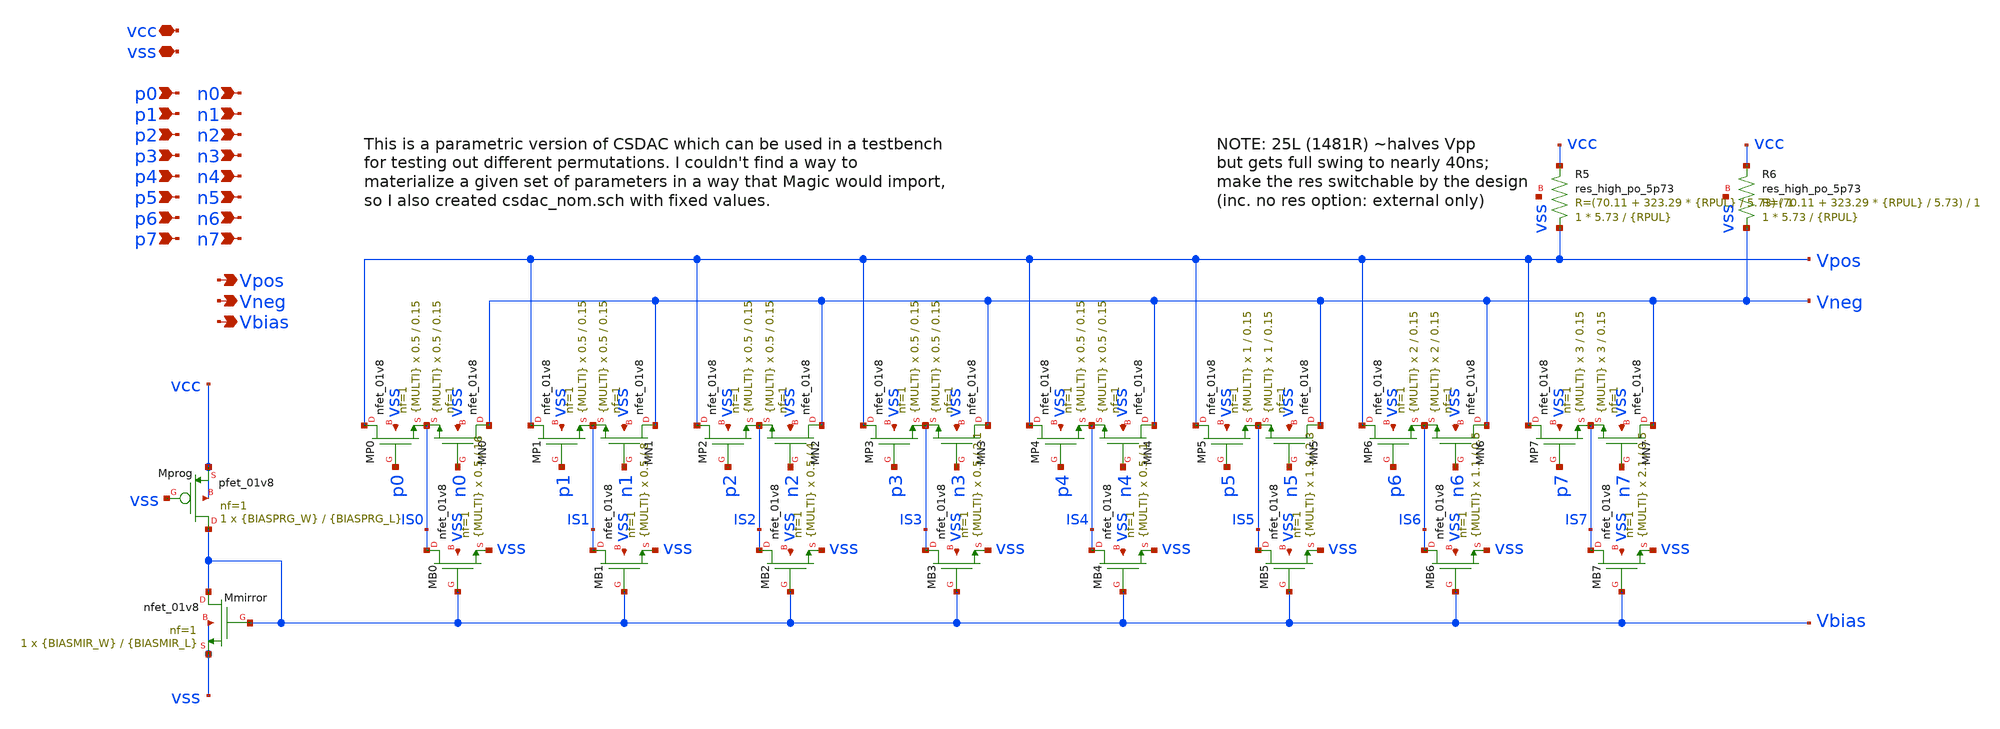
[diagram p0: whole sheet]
** sch_path: xschem/csdac.sch
**.subckt csdac vcc vss p0 n0 p1 n1 p2 n2 p3 n3 p4 n4 p5 n5 p6 n6 p7 n7 Vpos Vneg Vbias
*.iopin vcc
*.iopin vss
*.ipin p0
*.ipin n0
*.ipin p1
*.ipin n1
*.ipin p2
*.ipin n2
*.ipin p3
*.ipin n3
*.ipin p4
*.ipin n4
*.ipin p5
*.ipin n5
*.ipin p6
*.ipin n6
*.ipin p7
*.ipin n7
*.opin Vpos
*.opin Vneg
*.opin Vbias
XMprog Vbias vss vcc vcc sky130_fd_pr__pfet_01v8 L={BIASPRG_L} W={BIASPRG_W} nf=1 ad='int((nf+1)/2) * W/nf * 0.29'
+ as='int((nf+2)/2) * W/nf * 0.29' pd='2*int((nf+1)/2) * (W/nf + 0.29)' ps='2*int((nf+2)/2) * (W/nf + 0.29)'
+ nrd='0.29 / W' nrs='0.29 / W' sa=0 sb=0 sd=0 mult=1 m=1
XMmirror Vbias Vbias vss vss sky130_fd_pr__nfet_01v8 L={BIASMIR_L} W={BIASMIR_W} nf=1 ad='int((nf+1)/2) * W/nf * 0.29'
+ as='int((nf+2)/2) * W/nf * 0.29' pd='2*int((nf+1)/2) * (W/nf + 0.29)' ps='2*int((nf+2)/2) * (W/nf + 0.29)'
+ nrd='0.29 / W' nrs='0.29 / W' sa=0 sb=0 sd=0 mult=1 m=1
XMB0 IS0 Vbias vss vss sky130_fd_pr__nfet_01v8 L=16 W=0.5 nf=1 ad='int((nf+1)/2) * W/nf * 0.29' as='int((nf+2)/2) * W/nf * 0.29'
+ pd='2*int((nf+1)/2) * (W/nf + 0.29)' ps='2*int((nf+2)/2) * (W/nf + 0.29)' nrd='0.29 / W' nrs='0.29 / W'
+ sa=0 sb=0 sd=0 mult={MULTI} m={MULTI}
XMP0 Vpos p0 IS0 vss sky130_fd_pr__nfet_01v8 L=0.15 W=0.5 nf=1 ad='int((nf+1)/2) * W/nf * 0.29' as='int((nf+2)/2) * W/nf * 0.29'
+ pd='2*int((nf+1)/2) * (W/nf + 0.29)' ps='2*int((nf+2)/2) * (W/nf + 0.29)' nrd='0.29 / W' nrs='0.29 / W'
+ sa=0 sb=0 sd=0 mult={MULTI} m={MULTI}
XMN0 Vneg n0 IS0 vss sky130_fd_pr__nfet_01v8 L=0.15 W=0.5 nf=1 ad='int((nf+1)/2) * W/nf * 0.29' as='int((nf+2)/2) * W/nf * 0.29'
+ pd='2*int((nf+1)/2) * (W/nf + 0.29)' ps='2*int((nf+2)/2) * (W/nf + 0.29)' nrd='0.29 / W' nrs='0.29 / W'
+ sa=0 sb=0 sd=0 mult={MULTI} m={MULTI}
XMB1 IS1 Vbias vss vss sky130_fd_pr__nfet_01v8 L=8 W=0.5 nf=1 ad='int((nf+1)/2) * W/nf * 0.29' as='int((nf+2)/2) * W/nf * 0.29'
+ pd='2*int((nf+1)/2) * (W/nf + 0.29)' ps='2*int((nf+2)/2) * (W/nf + 0.29)' nrd='0.29 / W' nrs='0.29 / W'
+ sa=0 sb=0 sd=0 mult={MULTI} m={MULTI}
XMP1 Vpos p1 IS1 vss sky130_fd_pr__nfet_01v8 L=0.15 W=0.5 nf=1 ad='int((nf+1)/2) * W/nf * 0.29' as='int((nf+2)/2) * W/nf * 0.29'
+ pd='2*int((nf+1)/2) * (W/nf + 0.29)' ps='2*int((nf+2)/2) * (W/nf + 0.29)' nrd='0.29 / W' nrs='0.29 / W'
+ sa=0 sb=0 sd=0 mult={MULTI} m={MULTI}
XMN1 Vneg n1 IS1 vss sky130_fd_pr__nfet_01v8 L=0.15 W=0.5 nf=1 ad='int((nf+1)/2) * W/nf * 0.29' as='int((nf+2)/2) * W/nf * 0.29'
+ pd='2*int((nf+1)/2) * (W/nf + 0.29)' ps='2*int((nf+2)/2) * (W/nf + 0.29)' nrd='0.29 / W' nrs='0.29 / W'
+ sa=0 sb=0 sd=0 mult={MULTI} m={MULTI}
XMB2 IS2 Vbias vss vss sky130_fd_pr__nfet_01v8 L=4 W=0.5 nf=1 ad='int((nf+1)/2) * W/nf * 0.29' as='int((nf+2)/2) * W/nf * 0.29'
+ pd='2*int((nf+1)/2) * (W/nf + 0.29)' ps='2*int((nf+2)/2) * (W/nf + 0.29)' nrd='0.29 / W' nrs='0.29 / W'
+ sa=0 sb=0 sd=0 mult={MULTI} m={MULTI}
XMP2 Vpos p2 IS2 vss sky130_fd_pr__nfet_01v8 L=0.15 W=0.5 nf=1 ad='int((nf+1)/2) * W/nf * 0.29' as='int((nf+2)/2) * W/nf * 0.29'
+ pd='2*int((nf+1)/2) * (W/nf + 0.29)' ps='2*int((nf+2)/2) * (W/nf + 0.29)' nrd='0.29 / W' nrs='0.29 / W'
+ sa=0 sb=0 sd=0 mult={MULTI} m={MULTI}
XMN2 Vneg n2 IS2 vss sky130_fd_pr__nfet_01v8 L=0.15 W=0.5 nf=1 ad='int((nf+1)/2) * W/nf * 0.29' as='int((nf+2)/2) * W/nf * 0.29'
+ pd='2*int((nf+1)/2) * (W/nf + 0.29)' ps='2*int((nf+2)/2) * (W/nf + 0.29)' nrd='0.29 / W' nrs='0.29 / W'
+ sa=0 sb=0 sd=0 mult={MULTI} m={MULTI}
XMB3 IS3 Vbias vss vss sky130_fd_pr__nfet_01v8 L=2.1 W=0.5 nf=1 ad='int((nf+1)/2) * W/nf * 0.29' as='int((nf+2)/2) * W/nf * 0.29'
+ pd='2*int((nf+1)/2) * (W/nf + 0.29)' ps='2*int((nf+2)/2) * (W/nf + 0.29)' nrd='0.29 / W' nrs='0.29 / W'
+ sa=0 sb=0 sd=0 mult={MULTI} m={MULTI}
XMP3 Vpos p3 IS3 vss sky130_fd_pr__nfet_01v8 L=0.15 W=0.5 nf=1 ad='int((nf+1)/2) * W/nf * 0.29' as='int((nf+2)/2) * W/nf * 0.29'
+ pd='2*int((nf+1)/2) * (W/nf + 0.29)' ps='2*int((nf+2)/2) * (W/nf + 0.29)' nrd='0.29 / W' nrs='0.29 / W'
+ sa=0 sb=0 sd=0 mult={MULTI} m={MULTI}
XMN3 Vneg n3 IS3 vss sky130_fd_pr__nfet_01v8 L=0.15 W=0.5 nf=1 ad='int((nf+1)/2) * W/nf * 0.29' as='int((nf+2)/2) * W/nf * 0.29'
+ pd='2*int((nf+1)/2) * (W/nf + 0.29)' ps='2*int((nf+2)/2) * (W/nf + 0.29)' nrd='0.29 / W' nrs='0.29 / W'
+ sa=0 sb=0 sd=0 mult={MULTI} m={MULTI}
XMB4 IS4 Vbias vss vss sky130_fd_pr__nfet_01v8 L=1 W=0.5 nf=1 ad='int((nf+1)/2) * W/nf * 0.29' as='int((nf+2)/2) * W/nf * 0.29'
+ pd='2*int((nf+1)/2) * (W/nf + 0.29)' ps='2*int((nf+2)/2) * (W/nf + 0.29)' nrd='0.29 / W' nrs='0.29 / W'
+ sa=0 sb=0 sd=0 mult={MULTI} m={MULTI}
XMP4 Vpos p4 IS4 vss sky130_fd_pr__nfet_01v8 L=0.15 W=0.5 nf=1 ad='int((nf+1)/2) * W/nf * 0.29' as='int((nf+2)/2) * W/nf * 0.29'
+ pd='2*int((nf+1)/2) * (W/nf + 0.29)' ps='2*int((nf+2)/2) * (W/nf + 0.29)' nrd='0.29 / W' nrs='0.29 / W'
+ sa=0 sb=0 sd=0 mult={MULTI} m={MULTI}
XMN4 Vneg n4 IS4 vss sky130_fd_pr__nfet_01v8 L=0.15 W=0.5 nf=1 ad='int((nf+1)/2) * W/nf * 0.29' as='int((nf+2)/2) * W/nf * 0.29'
+ pd='2*int((nf+1)/2) * (W/nf + 0.29)' ps='2*int((nf+2)/2) * (W/nf + 0.29)' nrd='0.29 / W' nrs='0.29 / W'
+ sa=0 sb=0 sd=0 mult={MULTI} m={MULTI}
XMB5 IS5 Vbias vss vss sky130_fd_pr__nfet_01v8 L=2.3 W=1.9 nf=1 ad='int((nf+1)/2) * W/nf * 0.29' as='int((nf+2)/2) * W/nf * 0.29'
+ pd='2*int((nf+1)/2) * (W/nf + 0.29)' ps='2*int((nf+2)/2) * (W/nf + 0.29)' nrd='0.29 / W' nrs='0.29 / W'
+ sa=0 sb=0 sd=0 mult={MULTI} m={MULTI}
XMP5 Vpos p5 IS5 vss sky130_fd_pr__nfet_01v8 L=0.15 W=1 nf=1 ad='int((nf+1)/2) * W/nf * 0.29' as='int((nf+2)/2) * W/nf * 0.29'
+ pd='2*int((nf+1)/2) * (W/nf + 0.29)' ps='2*int((nf+2)/2) * (W/nf + 0.29)' nrd='0.29 / W' nrs='0.29 / W'
+ sa=0 sb=0 sd=0 mult={MULTI} m={MULTI}
XMN5 Vneg n5 IS5 vss sky130_fd_pr__nfet_01v8 L=0.15 W=1 nf=1 ad='int((nf+1)/2) * W/nf * 0.29' as='int((nf+2)/2) * W/nf * 0.29'
+ pd='2*int((nf+1)/2) * (W/nf + 0.29)' ps='2*int((nf+2)/2) * (W/nf + 0.29)' nrd='0.29 / W' nrs='0.29 / W'
+ sa=0 sb=0 sd=0 mult={MULTI} m={MULTI}
XMB6 IS6 Vbias vss vss sky130_fd_pr__nfet_01v8 L=0.5 W=1.1 nf=1 ad='int((nf+1)/2) * W/nf * 0.29' as='int((nf+2)/2) * W/nf * 0.29'
+ pd='2*int((nf+1)/2) * (W/nf + 0.29)' ps='2*int((nf+2)/2) * (W/nf + 0.29)' nrd='0.29 / W' nrs='0.29 / W'
+ sa=0 sb=0 sd=0 mult={MULTI} m={MULTI}
XMP6 Vpos p6 IS6 vss sky130_fd_pr__nfet_01v8 L=0.15 W=2 nf=1 ad='int((nf+1)/2) * W/nf * 0.29' as='int((nf+2)/2) * W/nf * 0.29'
+ pd='2*int((nf+1)/2) * (W/nf + 0.29)' ps='2*int((nf+2)/2) * (W/nf + 0.29)' nrd='0.29 / W' nrs='0.29 / W'
+ sa=0 sb=0 sd=0 mult={MULTI} m={MULTI}
XMN6 Vneg n6 IS6 vss sky130_fd_pr__nfet_01v8 L=0.15 W=2 nf=1 ad='int((nf+1)/2) * W/nf * 0.29' as='int((nf+2)/2) * W/nf * 0.29'
+ pd='2*int((nf+1)/2) * (W/nf + 0.29)' ps='2*int((nf+2)/2) * (W/nf + 0.29)' nrd='0.29 / W' nrs='0.29 / W'
+ sa=0 sb=0 sd=0 mult={MULTI} m={MULTI}
XMB7 IS7 Vbias vss vss sky130_fd_pr__nfet_01v8 L=0.5 W=2.1 nf=1 ad='int((nf+1)/2) * W/nf * 0.29' as='int((nf+2)/2) * W/nf * 0.29'
+ pd='2*int((nf+1)/2) * (W/nf + 0.29)' ps='2*int((nf+2)/2) * (W/nf + 0.29)' nrd='0.29 / W' nrs='0.29 / W'
+ sa=0 sb=0 sd=0 mult={MULTI} m={MULTI}
XMP7 Vpos p7 IS7 vss sky130_fd_pr__nfet_01v8 L=0.15 W=3 nf=1 ad='int((nf+1)/2) * W/nf * 0.29' as='int((nf+2)/2) * W/nf * 0.29'
+ pd='2*int((nf+1)/2) * (W/nf + 0.29)' ps='2*int((nf+2)/2) * (W/nf + 0.29)' nrd='0.29 / W' nrs='0.29 / W'
+ sa=0 sb=0 sd=0 mult={MULTI} m={MULTI}
XMN7 Vneg n7 IS7 vss sky130_fd_pr__nfet_01v8 L=0.15 W=3 nf=1 ad='int((nf+1)/2) * W/nf * 0.29' as='int((nf+2)/2) * W/nf * 0.29'
+ pd='2*int((nf+1)/2) * (W/nf + 0.29)' ps='2*int((nf+2)/2) * (W/nf + 0.29)' nrd='0.29 / W' nrs='0.29 / W'
+ sa=0 sb=0 sd=0 mult={MULTI} m={MULTI}
XR5 Vpos vcc vss sky130_fd_pr__res_high_po_5p73 L={RPUL} mult=1 m=1
XR6 Vneg vcc vss sky130_fd_pr__res_high_po_5p73 L={RPUL} mult=1 m=1
**.ends
.end
